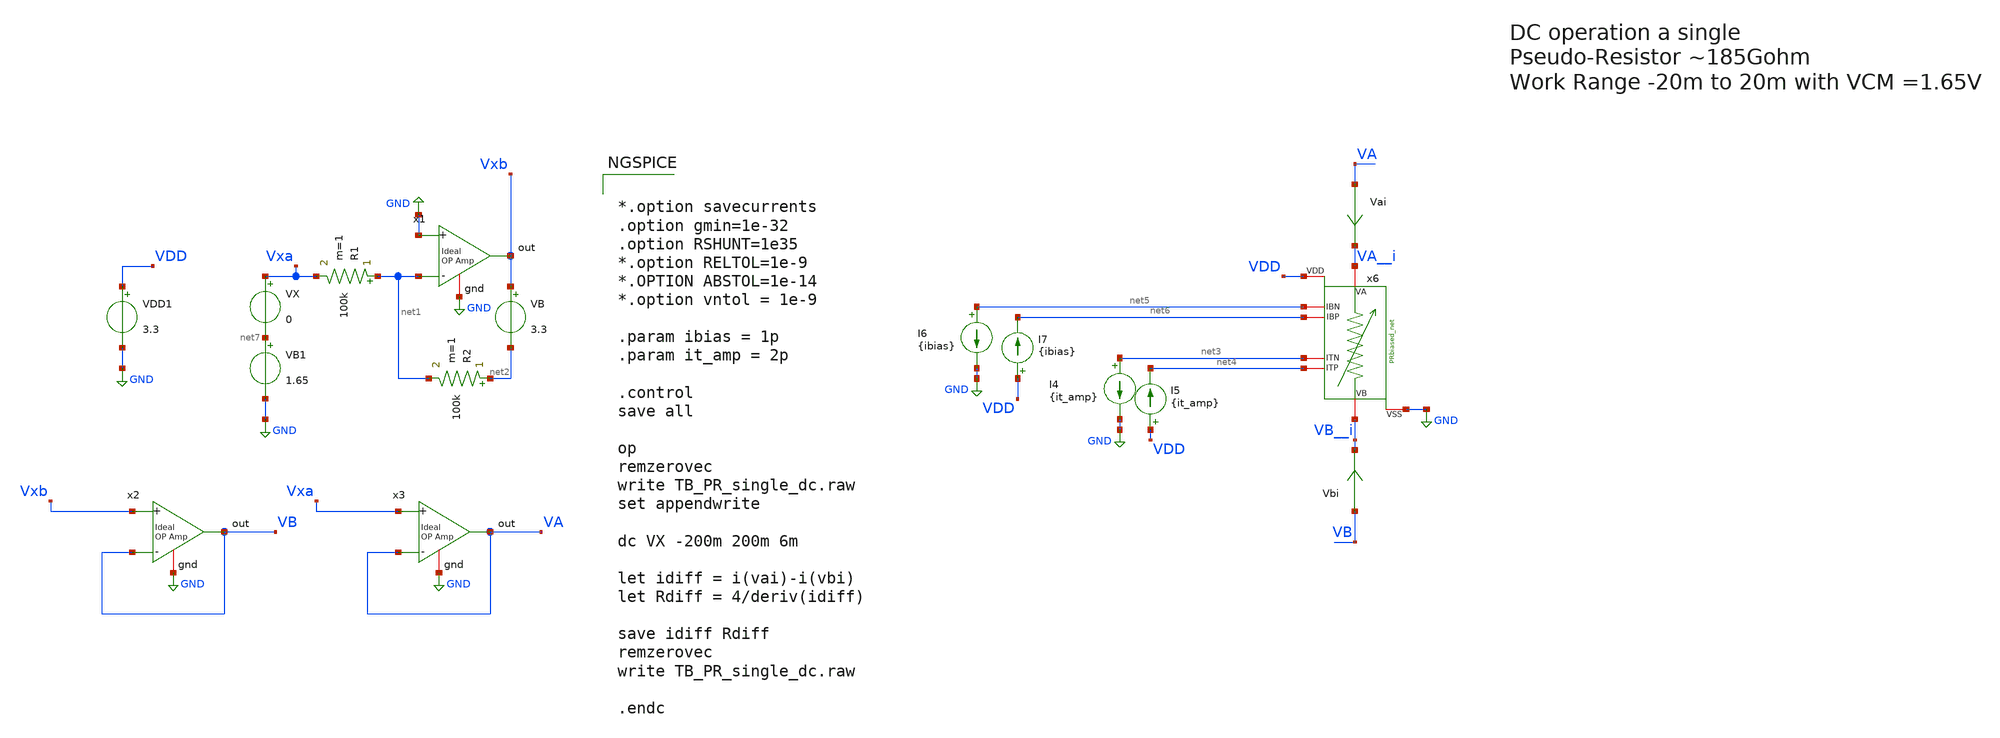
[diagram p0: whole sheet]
** sch_path: TIA_Filter/PseudoResistor/TB_PR_single_dc.sch
**.subckt TB_PR_single_dc
VDD1 VDD GND 3.3
VX Vxa net7 0
VB Vxb net2 3.3
R1 net1 Vxa 100k m=1
R2 net2 net1 100k m=1
VB1 net7 GND 1.65
x6 VA__i VB__i net5 net6 net3 net4 VDD GND PRbiased_net
I4 net3 GND {it_amp}
I5 VDD net4 {it_amp}
I6 net5 GND {ibias}
I7 VDD net6 {ibias}
Vai VA VA__i 0
.save i(vai)
Vbi VB VB__i 0
.save i(vbi)
x1 Vxb GND net1 GND ampOp_ideal
x2 VB Vxb VB GND ampOp_ideal
x3 VA Vxa VA GND ampOp_ideal
**** begin user architecture code

.include $::180MCU_MODELS/design.ngspice
.lib $::180MCU_MODELS/sm141064.ngspice typical





*.option savecurrents
.option gmin=1e-32
.option RSHUNT=1e35
*.option RELTOL=1e-9
*.OPTION ABSTOL=1e-14
*.option vntol = 1e-9

.param ibias = 1p
.param it_amp = 2p

.control
save all

op
remzerovec
write TB_PR_single_dc.raw
set appendwrite

dc VX -200m 200m 6m

let idiff = i(vai)-i(vbi)
let Rdiff = 4/deriv(idiff)

save idiff Rdiff
remzerovec
write TB_PR_single_dc.raw

.endc


**** end user architecture code
**.ends
.GLOBAL GND
.end
